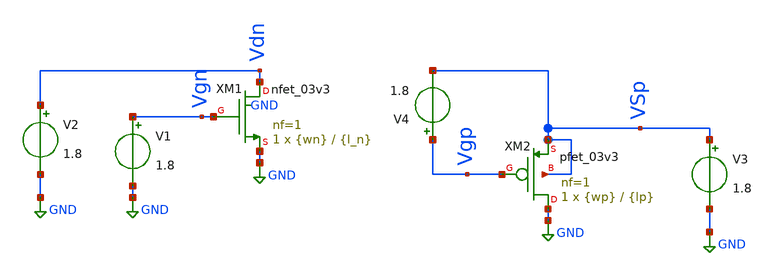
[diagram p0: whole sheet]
** sch_path: xschem/caracterizador/charac.sch
* Copyright 2022 GlobalFoundries PDK Authors
* Licensed under the Apache License, Version 2.0 (the "License");
* you may not use this file except in compliance with the License.
* You may obtain a copy of the License at
* https://www.apache.org/licenses/LICENSE-2.0
* Unless required by applicable law or agreed to in writing, software
* distributed under the License is distributed on an "AS IS" BASIS,
* WITHOUT WARRANTIES OR CONDITIONS OF ANY KIND, either express or implied.
* See the License for the specific language governing permissions and
* limitations under the License.
**.subckt charac
XM1 Vdn Vgn GND GND nfet_03v3 L={l_n} W={wn} nf=1 ad='int((nf+1)/2) * W/nf * 0.18u' as='int((nf+2)/2) * W/nf * 0.18u'
+ pd='2*int((nf+1)/2) * (W/nf + 0.18u)' ps='2*int((nf+2)/2) * (W/nf + 0.18u)' nrd='0.18u / W' nrs='0.18u / W'
+ sa=0 sb=0 sd=0 m=1 par=1
XM2 GND Vgp VSp VSp pfet_03v3 L={lp} W={wp} nf=1 ad='int((nf+1)/2) * W/nf * 0.18u' as='int((nf+2)/2) * W/nf * 0.18u'
+ pd='2*int((nf+1)/2) * (W/nf + 0.18u)' ps='2*int((nf+2)/2) * (W/nf + 0.18u)' nrd='0.18u / W' nrs='0.18u / W'
+ sa=0 sb=0 sd=0 m=1 par=1
V1 Vgn GND 1.8
V2 Vdn GND 1.8
V3 VSp GND 1.8
V4 Vgp VSp 1.8
**** begin user architecture code


.include /home/ringosinye/eda/pdks/gf180mcuD/libs.tech/ngspice/design.ngspice
.lib /home/ringosinye/eda/pdks/gf180mcuD/libs.tech/ngspice/sm141064.ngspice typical
.param sw_stat_mismatch = 0
.param wn=1u l_n=1u wp=1u lp=1u




.control

* ========================================================
* 1. PARAMETROS EDITABLES
* ========================================================
* --- NMOS: dimensiones (m) y punto de polarizacion (V) ---
set wn_val = 1e-6
set ln_val = 1e-6
set vgs_n = 0.723807
set vds_n = 1.3

* --- PMOS: dimensiones (m) y punto de polarizacion (V, magnitudes) ---
set wp_val = 1e-6
set lp_val = 1e-6
set vsg_p = 0.939722
set vsd_p = 960e-3

* Aplicar W y L al circuito
alterparam wn=$wn_val
alterparam l_n=$ln_val
alterparam wp=$wp_val
alterparam lp=$lp_val
reset

* Guardar nodos, fuentes y TODOS los parametros internos BSIM4 necesarios
save all

* Guardar parámetros internos del NMOS (XM1)
save @m.xm1.m0[id]
save @m.xm1.m0[vth]
save @m.xm1.m0[vdsat]
save @m.xm1.m0[gm]
save @m.xm1.m0[gds]
save @m.xm1.m0[gmbs]
save @m.xm1.m0[cgg]
save @m.xm1.m0[cgs]
save @m.xm1.m0[cgd]

*Guardar parámetros internos del PMOS (XM2)
save @m.xm2.m0[id]
save @m.xm2.m0[vth]
save @m.xm2.m0[vdsat]
save @m.xm2.m0[gm]
save @m.xm2.m0[gds]
save @m.xm2.m0[gmbs]
save @m.xm2.m0[cgg]
save @m.xm2.m0[cgs]
save @m.xm2.m0[cgd]

* ========================================================
* 2. UNICO PUNTO DE OPERACION (NMOS y PMOS)
* ========================================================
set vgs_p_neg = -$vsg_p
alter v1 $vgs_n
alter v2 $vds_n
alter v4 $vgs_p_neg
alter v3 $vsd_p
op

* ========================================================
* 3. EXTRACCION DIRECTA BSIM4 Y CALCULOS DERIVADOS (NMOS)
* ========================================================
let id_n_x    = abs(@m.xm1.m0[id])
let vth_n_x   = abs(@m.xm1.m0[vth])
let vdsat_n_x = abs(@m.xm1.m0[vdsat])
let gm_n_x    = abs(@m.xm1.m0[gm])
let gds_n_x   = abs(@m.xm1.m0[gds])
let gmb_n_x   = abs(@m.xm1.m0[gmbs])
let cgg_n_x   = abs(@m.xm1.m0[cgg])
let cgs_n_x   = abs(@m.xm1.m0[cgs])
let cgd_n_x   = abs(@m.xm1.m0[cgd])

set id_n_val    = $&id_n_x
set vth_n_val   = $&vth_n_x
set vdsat_n_val = $&vdsat_n_x
set gm_n_val    = $&gm_n_x
set gds_n_val   = $&gds_n_x
set gmb_n_val   = $&gmb_n_x
set cgg_n_val   = $&cgg_n_x
set cgs_n_val   = $&cgs_n_x
set cgd_n_val   = $&cgd_n_x

* Calculos derivados NMOS
let vov_n       = $vgs_n - $vth_n_val
let vdsmvdsat_n = $vds_n - $vdsat_n_val
let ro_n        = 1 / $gds_n_val
let gmro_n      = $gm_n_val / $gds_n_val
let gmoid_n     = $gm_n_val / $id_n_val
let ft_n        = $gm_n_val / (2*pi*$cgg_n_val)
let ftgmid_n    = ft_n * gmoid_n
let gft_n       = ft_n * gmro_n

set vov_n_val       = $&vov_n
set vdsmvdsat_n_val = $&vdsmvdsat_n
set ro_n_val        = $&ro_n
set gmro_n_val      = $&gmro_n
set gmoid_n_val     = $&gmoid_n
set ft_n_val        = $&ft_n
set ftgmid_n_val    = $&ftgmid_n
set gft_n_val       = $&gft_n

set region_n = 2
if $vgs_n < $vth_n_val
  set region_n = 3
else
  if $vds_n < $vdsat_n_val
    set region_n = 1
  end
end

* ========================================================
* 4. EXTRACCION DIRECTA BSIM4 Y CALCULOS DERIVADOS (PMOS)
* ========================================================
let id_p_x    = abs(@m.xm2.m0[id])
let vth_p_x   = abs(@m.xm2.m0[vth])
let vdsat_p_x = abs(@m.xm2.m0[vdsat])
let gm_p_x    = abs(@m.xm2.m0[gm])
let gds_p_x   = abs(@m.xm2.m0[gds])
let gmb_p_x   = abs(@m.xm2.m0[gmbs])
let cgg_p_x   = abs(@m.xm2.m0[cgg])
let cgs_p_x   = abs(@m.xm2.m0[cgs])
let cgd_p_x   = abs(@m.xm2.m0[cgd])

set id_p_val    = $&id_p_x
set vth_p_val   = $&vth_p_x
set vdsat_p_val = $&vdsat_p_x
set gm_p_val    = $&gm_p_x
set gds_p_val   = $&gds_p_x
set gmb_p_val   = $&gmb_p_x
set cgg_p_val   = $&cgg_p_x
set cgs_p_val   = $&cgs_p_x
set cgd_p_val   = $&cgd_p_x

* Calculos derivados PMOS
let vov_p       = $vsg_p - $vth_p_val
let vdsmvdsat_p = $vsd_p - $vdsat_p_val
let ro_p        = 1 / $gds_p_val
let gmro_p      = $gm_p_val / $gds_p_val
let gmoid_p     = $gm_p_val / $id_p_val
let ft_p        = $gm_p_val / (2*pi*$cgg_p_val)
let ftgmid_p    = ft_p * gmoid_p
let gft_p       = ft_p * gmro_p

set vov_p_val       = $&vov_p
set vdsmvdsat_p_val = $&vdsmvdsat_p
set ro_p_val        = $&ro_p
set gmro_p_val      = $&gmro_p
set gmoid_p_val     = $&gmoid_p
set ft_p_val        = $&ft_p
set ftgmid_p_val    = $&ftgmid_p
set gft_p_val       = $&gft_p

set region_p = 2
if $vsg_p < $vth_p_val
  set region_p = 3
else
  if $vsd_p < $vdsat_p_val
    set region_p = 1
  end
end

* ========================================================
* 5. IMPRESION DE TABLAS (ORDEN EXACTO CADENCE ADE)
* ========================================================
echo ==========================================================
echo  NMOS (XM1) : W = $wn_val m | L = $ln_val m
echo ==========================================================
echo  ID          = $id_n_val A
echo  VGS         = $vgs_n V
echo  VDS         = $vds_n V
echo  VSB         = 0 V
echo  VTH         = $vth_n_val V
echo  Vov         = $vov_n_val V
echo  Vdsat       = $vdsat_n_val V
echo  VDS-Vdsat   = $vdsmvdsat_n_val V
echo  Region      = $region_n (1:triodo, 2:sat, 3:subumbral)
echo  gm          = $gm_n_val S
echo  ro          = $ro_n_val Ohm
echo  gmb         = $gmb_n_val S
echo  gmro        = $gmro_n_val V/V
echo  Cgs         = $cgs_n_val F
echo  Cgd         = $cgd_n_val F
echo  gmoid       = $gmoid_n_val 1/V
echo  fT          = $ft_n_val Hz
echo  FTGMID      = $ftgmid_n_val Hz/V
echo  GFT         = $gft_n_val Hz
echo ==========================================================
echo
echo ==========================================================
echo  PMOS (XM2) : W = $wp_val m | L = $lp_val m  (magnitudes)
echo ==========================================================
echo  ID          = $id_p_val A
echo  VSG         = $vsg_p V
echo  VSD         = $vsd_p V
echo  VSB         = 0 V
echo  VTH         = $vth_p_val V
echo  Vov         = $vov_p_val V
echo  Vdsat       = $vdsat_p_val V
echo  VSD-Vdsat   = $vdsmvdsat_p_val V
echo  Region      = $region_p (1:triodo, 2:sat, 3:subumbral)
echo  gm          = $gm_p_val S
echo  ro          = $ro_p_val Ohm
echo  gmb         = $gmb_p_val S
echo  gmro        = $gmro_p_val V/V
echo  Cgs         = $cgs_p_val F
echo  Cgd         = $cgd_p_val F
echo  gmoid       = $gmoid_p_val 1/V
echo  fT          = $ft_p_val Hz
echo  FTGMID      = $ftgmid_p_val Hz/V
echo  GFT         = $gft_p_val Hz
echo ==========================================================
.endc


**** end user architecture code
**.ends
.GLOBAL GND
.end
